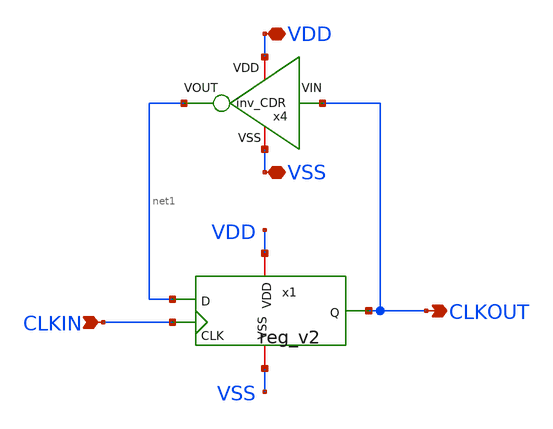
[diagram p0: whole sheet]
** sch_path: CDR4176-main/schematic/xschem/div_freq_x2/div_freq_x2.sch
**.subckt div_freq_x2 VDD VSS CLKIN CLKOUT
*.iopin VDD
*.iopin VSS
*.ipin CLKIN
*.opin CLKOUT
x1 VDD CLKIN VSS CLKOUT net1 reg_v2
x4 VDD net1 CLKOUT VSS inv_CDR
**.ends

* expanding   symbol:  reg_v2/reg_v2.sym # of pins=5
** sym_path: CDR4176-main/schematic/xschem/reg_v2/reg_v2.sym
** sch_path: CDR4176-main/schematic/xschem/reg_v2/reg_v2.sch
.subckt reg_v2 VDD CLK VSS Q D
*.iopin VDD
*.iopin VSS
*.ipin CLK
*.ipin D
*.opin Q
x3 net7 CLK CLK_B net2 VDD VSS tg_custom
x9 VDD CLK_B CLK VSS inv_CDR
x4 VDD net2 net1 VSS inv_CDR
x8 VDD net4 D VSS inv_CDR
x11 VDD net3 Q VSS inv_CDR
x10 VDD net5 net1 VSS inv_CDR
x2 net7 CLK_B CLK net4 VDD VSS tg_custom
x6 net6 CLK_B CLK net3 VDD VSS tg_custom
x7 net6 CLK CLK_B net5 VDD VSS tg_custom
x5 VDD net1 net7 VSS inv_CDR
x1 VDD Q net6 VSS inv_CDR
.ends


* expanding   symbol:  inv_CDR/inv_CDR.sym # of pins=4
** sym_path: CDR4176-main/schematic/xschem/inv_CDR/inv_CDR.sym
** sch_path: CDR4176-main/schematic/xschem/inv_CDR/inv_CDR.sch
.subckt inv_CDR VDD VOUT VIN VSS
*.iopin VDD
*.iopin VSS
*.opin VOUT
*.ipin VIN
XM2 VOUT VIN VDD VDD sg13_lv_pmos w=0.15u l=0.13u ng=1 m=1 mm_ok=1
XM1 VOUT VIN VSS VSS sg13_lv_nmos w=0.15u l=0.13u ng=1 m=1 mm_ok=1
.ends


* expanding   symbol:  tg_custom/tg_custom.sym # of pins=6
** sym_path: CDR4176-main/schematic/xschem/tg_custom/tg_custom.sym
** sch_path: CDR4176-main/schematic/xschem/tg_custom/tg_custom.sch
.subckt tg_custom VOUT VSN VSP VIN VBP VBN
*.iopin VIN
*.iopin VSN
*.iopin VOUT
*.iopin VSP
*.iopin VBN
*.iopin VBP
XM1 VOUT VSN VIN VBN sg13_lv_nmos w=0.15u l=0.13u ng=1 m=1 mm_ok=1
XM2 VOUT VSP VIN VBP sg13_lv_pmos w=0.3u l=0.13u ng=2 m=1 mm_ok=1
.ends

.end
